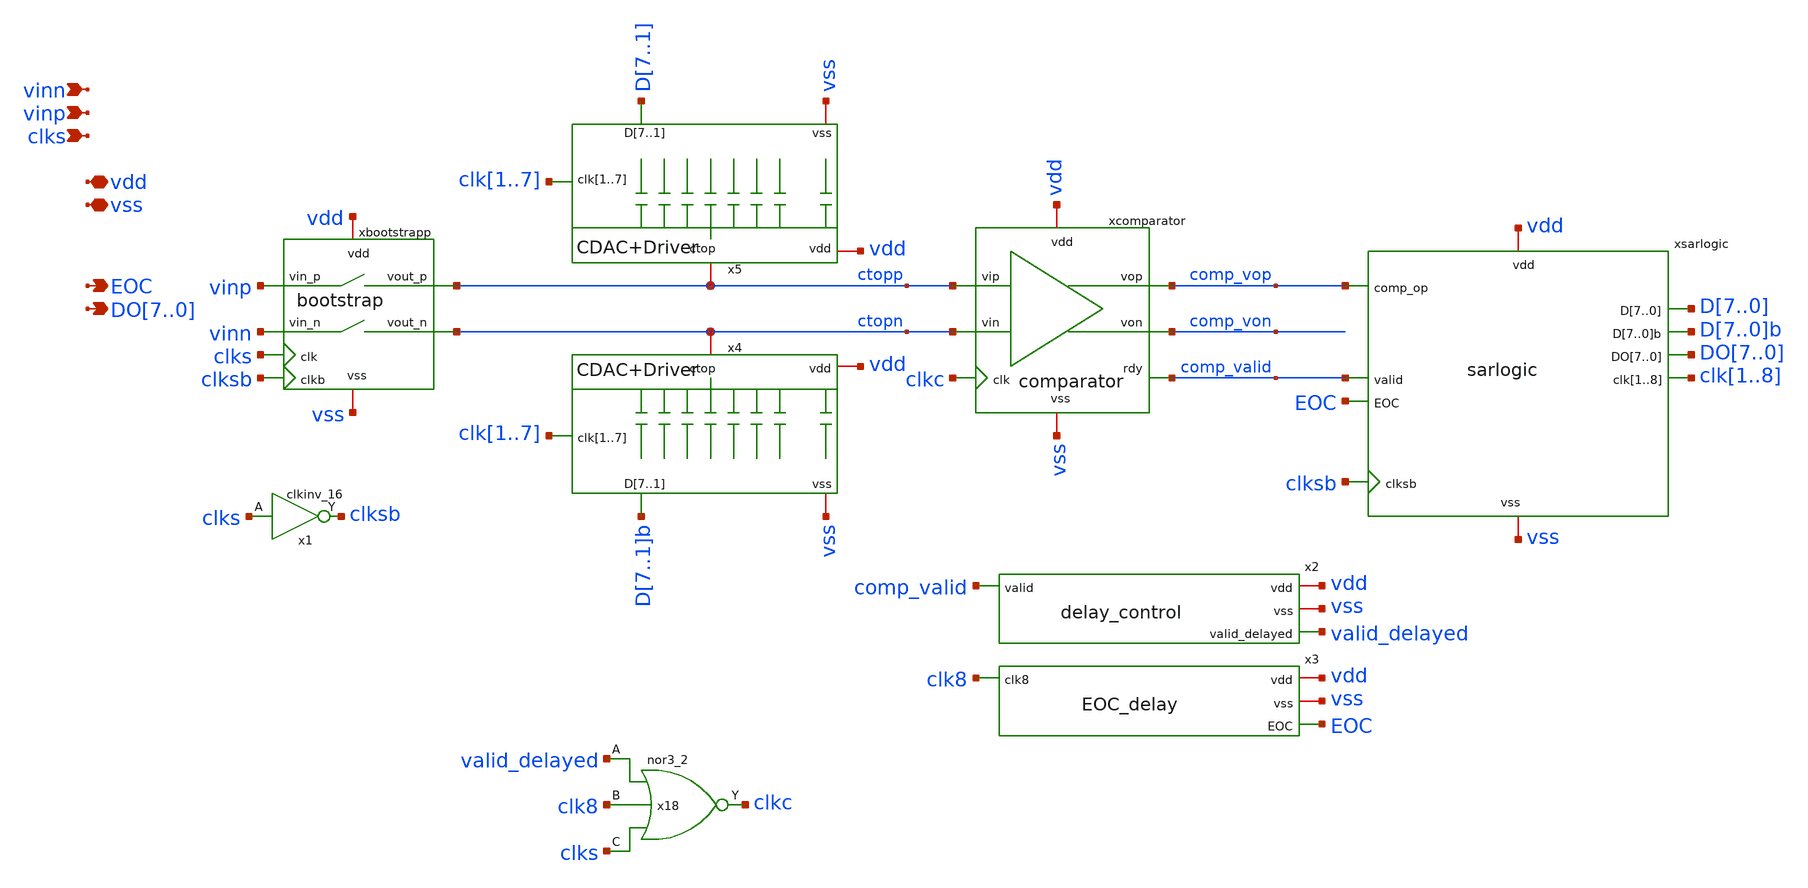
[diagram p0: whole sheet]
** sch_path: xschem/sar-adc/sar-adc.sch
**.subckt sar-adc vinn vinp clks EOC vdd vss DO7,DO6,DO5,DO4,DO3,DO2,DO1,DO0
*.ipin vinn
*.ipin vinp
*.ipin clks
*.opin EOC
*.iopin vdd
*.iopin vss
*.opin DO7,DO6,DO5,DO4,DO3,DO2,DO1,DO0
xcomparator vdd comp_vop clkc comp_von ctopp ctopn vss comp_valid comparator
xsarlogic vdd vss D7 D6 D5 D4 D3 D2 D1 D0 comp_valid comp_vop D7b D6b D5b D4b D3b D2b D1b D0b clk1
+ clk2 clk3 clk4 clk5 clk6 clk7 clk8 DO7 DO6 DO5 DO4 DO3 DO2 DO1 DO0 clksb EOC sarlogic
xbootstrapp clks vinp ctopp vdd vss vinn ctopn clksb bootstrap
x1 clks vss vss vdd vdd clksb sky130_fd_sc_hd__clkinv_16
x2 vdd vss comp_valid valid_delayed delay_control
x18 valid_delayed clk8 clks vss vss vdd vdd clkc sky130_fd_sc_hd__nor3_2
x4 vdd clk1 clk2 clk3 clk4 clk5 clk6 clk7 D7b D6b D5b D4b D3b D2b D1b ctopn vss CDAC+Driver
x5 vdd clk1 clk2 clk3 clk4 clk5 clk6 clk7 D7 D6 D5 D4 D3 D2 D1 ctopp vss CDAC+Driver
x3 vdd vss clk8 EOC EOC_delay
**.ends
.end
